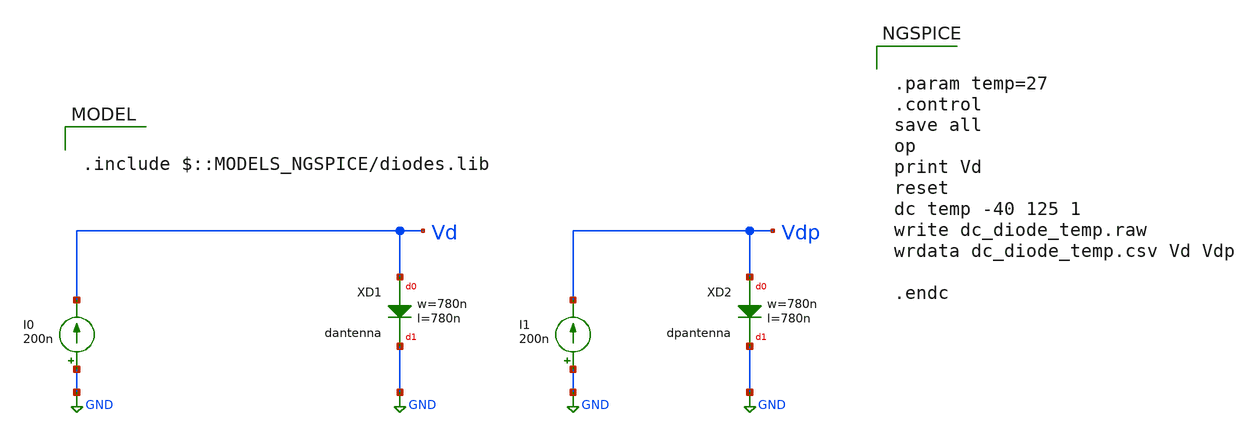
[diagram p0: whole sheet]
** sch_path: ihp-sg13g2/xschem_libs/sg13g2_tests/dc_diode_temp/schematic/dc_diode_temp.sch
* Copyright 2023 IHP PDK Authors
**.subckt dc_diode_temp
XXD1 Vd GND dantenna l=780n w=780n
I0 GND Vd 200n
I1 GND Vdp 200n
XXD2 Vdp GND dpantenna l=780n w=780n
**** begin user architecture code

.include $::MODELS_NGSPICE/diodes.lib



.param temp=27
.control
save all
op
print Vd
reset
dc temp -40 125 1
write dc_diode_temp.raw
wrdata dc_diode_temp.csv Vd Vdp

.endc


**** end user architecture code
**.ends
.GLOBAL GND
.end
